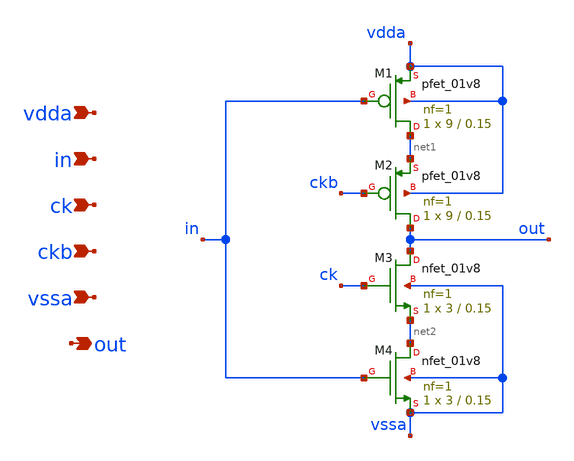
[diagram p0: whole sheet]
** sch_path: xschem/dac_sw.sch
**.subckt dac_sw vdda in ck ckb vssa out
*.ipin vdda
*.ipin in
*.ipin ck
*.ipin ckb
*.ipin vssa
*.opin out
XM1 net1 in vdda vdda sky130_fd_pr__pfet_01v8 L=0.15 W=9 nf=1 ad='int((nf+1)/2) * W/nf * 0.29' as='int((nf+2)/2) * W/nf * 0.29'
+ pd='2*int((nf+1)/2) * (W/nf + 0.29)' ps='2*int((nf+2)/2) * (W/nf + 0.29)' nrd='0.29 / W' nrs='0.29 / W'
+ sa=0 sb=0 sd=0 mult=1 m=1
XM2 out ckb net1 vdda sky130_fd_pr__pfet_01v8 L=0.15 W=9 nf=1 ad='int((nf+1)/2) * W/nf * 0.29' as='int((nf+2)/2) * W/nf * 0.29'
+ pd='2*int((nf+1)/2) * (W/nf + 0.29)' ps='2*int((nf+2)/2) * (W/nf + 0.29)' nrd='0.29 / W' nrs='0.29 / W'
+ sa=0 sb=0 sd=0 mult=1 m=1
XM3 out ck net2 vssa sky130_fd_pr__nfet_01v8 L=0.15 W=3 nf=1 ad='int((nf+1)/2) * W/nf * 0.29' as='int((nf+2)/2) * W/nf * 0.29'
+ pd='2*int((nf+1)/2) * (W/nf + 0.29)' ps='2*int((nf+2)/2) * (W/nf + 0.29)' nrd='0.29 / W' nrs='0.29 / W'
+ sa=0 sb=0 sd=0 mult=1 m=1
XM4 net2 in vssa vssa sky130_fd_pr__nfet_01v8 L=0.15 W=3 nf=1 ad='int((nf+1)/2) * W/nf * 0.29' as='int((nf+2)/2) * W/nf * 0.29'
+ pd='2*int((nf+1)/2) * (W/nf + 0.29)' ps='2*int((nf+2)/2) * (W/nf + 0.29)' nrd='0.29 / W' nrs='0.29 / W'
+ sa=0 sb=0 sd=0 mult=1 m=1
**.ends
.end
